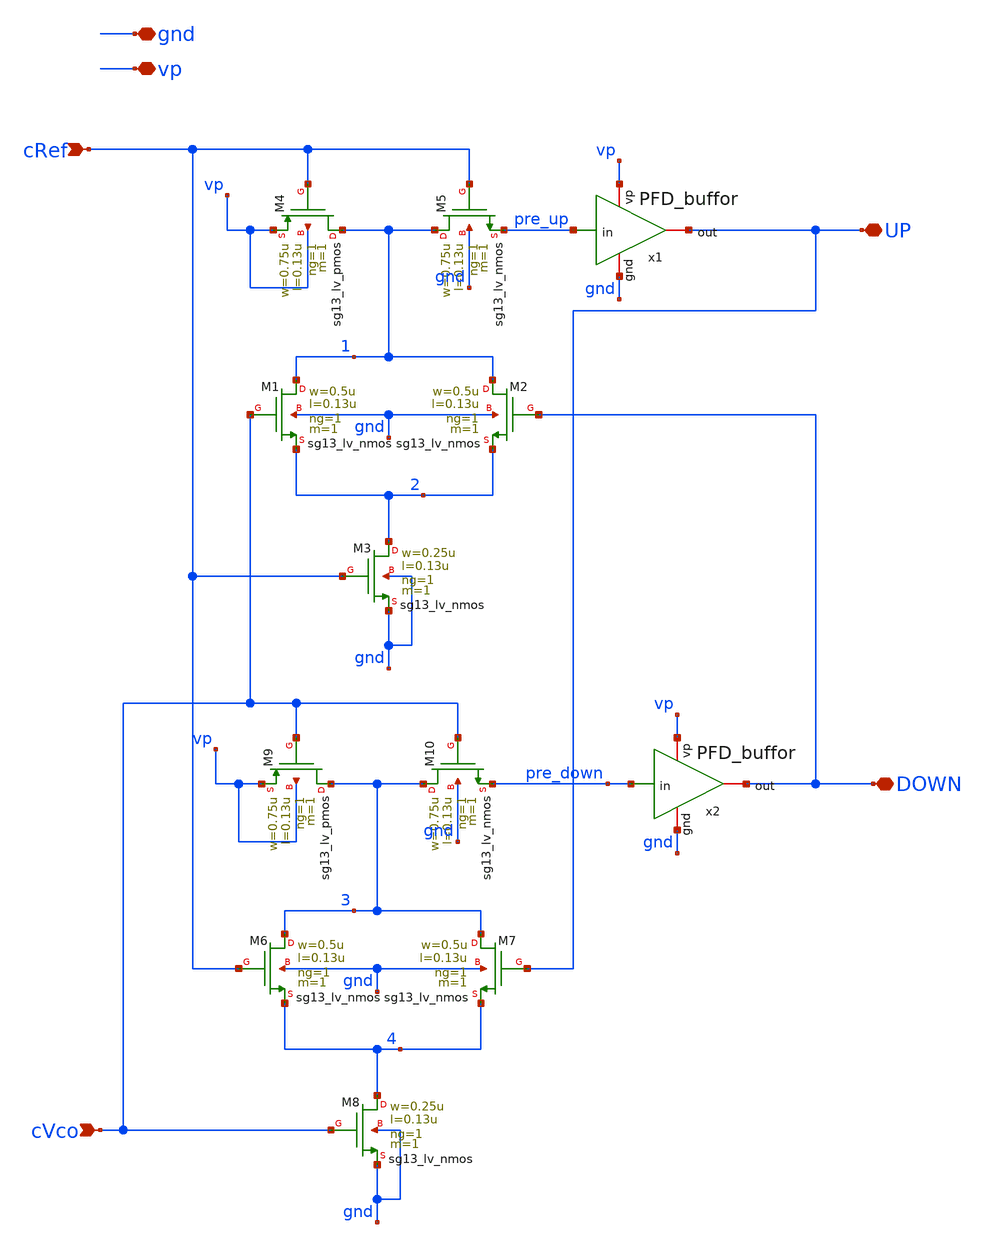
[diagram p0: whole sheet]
** sch_path: PFD/PFD_cell.sch
**.subckt PFD_cell gnd vp DOWN UP cRef cVco
*.iopin gnd
*.iopin vp
*.iopin DOWN
*.iopin UP
*.ipin cRef
*.ipin cVco
XM1 1 cVco 2 gnd sg13_lv_nmos w=0.5u l=0.13u ng=1 m=1 mm_ok=1
XM2 1 DOWN 2 gnd sg13_lv_nmos w=0.5u l=0.13u ng=1 m=1 mm_ok=1
XM3 2 cRef gnd gnd sg13_lv_nmos w=0.25u l=0.13u ng=1 m=1 mm_ok=1
XM4 1 cRef vp vp sg13_lv_pmos w=0.75u l=0.13u ng=1 m=1 mm_ok=1
XM6 3 cRef 4 gnd sg13_lv_nmos w=0.5u l=0.13u ng=1 m=1 mm_ok=1
XM7 3 UP 4 gnd sg13_lv_nmos w=0.5u l=0.13u ng=1 m=1 mm_ok=1
XM8 4 cVco gnd gnd sg13_lv_nmos w=0.25u l=0.13u ng=1 m=1 mm_ok=1
XM9 3 cVco vp vp sg13_lv_pmos w=0.75u l=0.13u ng=1 m=1 mm_ok=1
x1 gnd vp UP pre_up PFD_buffor
x2 gnd vp DOWN pre_down PFD_buffor
XM5 1 cRef pre_up gnd sg13_lv_nmos w=0.75u l=0.13u ng=1 m=1 mm_ok=1
XM10 3 cVco pre_down gnd sg13_lv_nmos w=0.75u l=0.13u ng=1 m=1 mm_ok=1
**.ends

* expanding   symbol:  PFD_buffor.sym # of pins=4
** sym_path: schematics/PFD/PFD_buffor.sym
** sch_path: schematics/PFD/PFD_buffor.sch
.subckt PFD_buffor gnd vp out in
*.iopin gnd
*.iopin vp
*.ipin in
*.iopin out
XM1 out_stage1 in gnd gnd sg13_lv_nmos w=0.3u l=0.15u ng=1 m=1 mm_ok=1
XM4 out_stage1 in vp vp sg13_lv_pmos w=0.3u l=0.15u ng=1 m=1 mm_ok=1
XM2 out out_stage1 gnd gnd sg13_lv_nmos w=0.6u l=0.15u ng=1 m=1 mm_ok=1
XM3 out out_stage1 vp vp sg13_lv_pmos w=0.6u l=0.15u ng=1 m=1 mm_ok=1
.ends

.end
